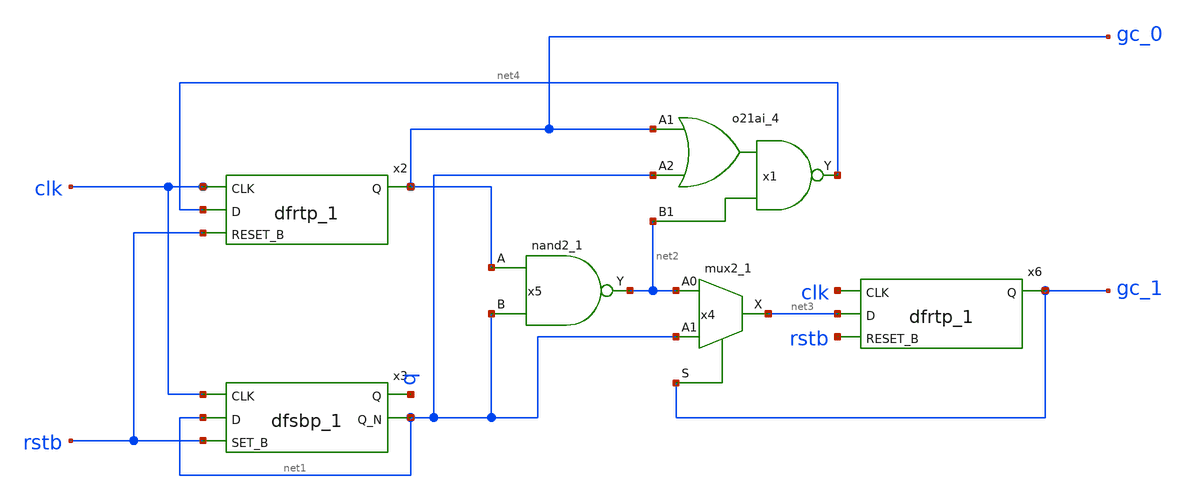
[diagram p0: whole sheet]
** sch_path: xschem/untitled-1.sch
**.subckt untitled-1
x1 gc_0 net1 net2 GND GND VDD VDD net4 sky130_fd_sc_hd__o21ai_4
x2 clk net4 rstb GND GND VDD VDD gc_0 sky130_fd_sc_hd__dfrtp_1
x4 net2 net1 gc_1 GND GND VDD VDD net3 sky130_fd_sc_hd__mux2_1
x5 gc_0 net1 GND GND VDD VDD net2 sky130_fd_sc_hd__nand2_1
x3 clk net1 rstb GND GND VDD VDD q net1 sky130_fd_sc_hd__dfsbp_1
x6 clk net3 rstb GND GND VDD VDD gc_1 sky130_fd_sc_hd__dfrtp_1
**.ends
.end
